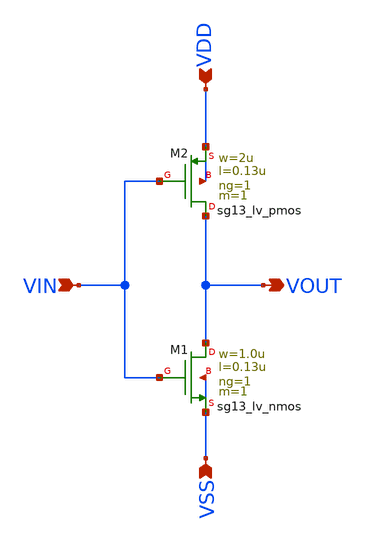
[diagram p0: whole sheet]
** sch_path: OSC9996-main/schematic/xschem/gate_inv_L0d13.sch
**.subckt gate_inv_L0d13 VDD VSS VIN VOUT
*.ipin VDD
*.ipin VSS
*.ipin VIN
*.opin VOUT
XM2 VOUT VIN VDD VDD sg13_lv_pmos w=2u l=0.13u ng=1 m=1 mm_ok=1
XM1 VOUT VIN VSS VSS sg13_lv_nmos w=1.0u l=0.13u ng=1 m=1 mm_ok=1
**.ends
.end
